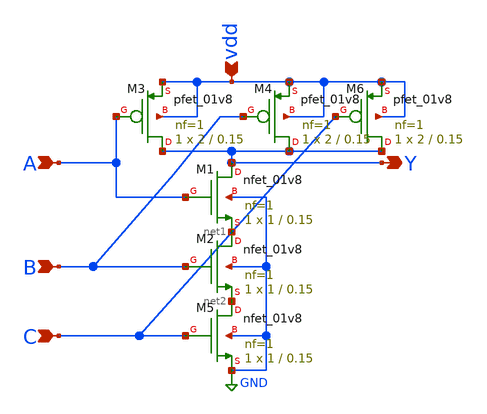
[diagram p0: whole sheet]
** sch_path: Circuit Files/Logic gate design using MOSFETS/gates/3_NAND_GATE.sch
**.subckt 3_NAND_GATE A B Y vdd C
*.ipin A
*.ipin B
*.opin Y
*.ipin vdd
*.ipin C
XM1 Y A net1 GND sky130_fd_pr__nfet_01v8 L=0.15 W=1 nf=1 ad='int((nf+1)/2) * W/nf * 0.29' as='int((nf+2)/2) * W/nf * 0.29'
+ pd='2*int((nf+1)/2) * (W/nf + 0.29)' ps='2*int((nf+2)/2) * (W/nf + 0.29)' nrd='0.29 / W' nrs='0.29 / W'
+ sa=0 sb=0 sd=0 mult=1 m=1
XM2 net1 B net2 GND sky130_fd_pr__nfet_01v8 L=0.15 W=1 nf=1 ad='int((nf+1)/2) * W/nf * 0.29' as='int((nf+2)/2) * W/nf * 0.29'
+ pd='2*int((nf+1)/2) * (W/nf + 0.29)' ps='2*int((nf+2)/2) * (W/nf + 0.29)' nrd='0.29 / W' nrs='0.29 / W'
+ sa=0 sb=0 sd=0 mult=1 m=1
XM3 Y A vdd vdd sky130_fd_pr__pfet_01v8 L=0.15 W=2 nf=1 ad='int((nf+1)/2) * W/nf * 0.29' as='int((nf+2)/2) * W/nf * 0.29'
+ pd='2*int((nf+1)/2) * (W/nf + 0.29)' ps='2*int((nf+2)/2) * (W/nf + 0.29)' nrd='0.29 / W' nrs='0.29 / W'
+ sa=0 sb=0 sd=0 mult=1 m=1
XM4 Y B vdd vdd sky130_fd_pr__pfet_01v8 L=0.15 W=2 nf=1 ad='int((nf+1)/2) * W/nf * 0.29' as='int((nf+2)/2) * W/nf * 0.29'
+ pd='2*int((nf+1)/2) * (W/nf + 0.29)' ps='2*int((nf+2)/2) * (W/nf + 0.29)' nrd='0.29 / W' nrs='0.29 / W'
+ sa=0 sb=0 sd=0 mult=1 m=1
XM5 net2 C GND GND sky130_fd_pr__nfet_01v8 L=0.15 W=1 nf=1 ad='int((nf+1)/2) * W/nf * 0.29' as='int((nf+2)/2) * W/nf * 0.29'
+ pd='2*int((nf+1)/2) * (W/nf + 0.29)' ps='2*int((nf+2)/2) * (W/nf + 0.29)' nrd='0.29 / W' nrs='0.29 / W'
+ sa=0 sb=0 sd=0 mult=1 m=1
XM6 Y C vdd vdd sky130_fd_pr__pfet_01v8 L=0.15 W=2 nf=1 ad='int((nf+1)/2) * W/nf * 0.29' as='int((nf+2)/2) * W/nf * 0.29'
+ pd='2*int((nf+1)/2) * (W/nf + 0.29)' ps='2*int((nf+2)/2) * (W/nf + 0.29)' nrd='0.29 / W' nrs='0.29 / W'
+ sa=0 sb=0 sd=0 mult=1 m=1
**.ends
.GLOBAL GND
.end
